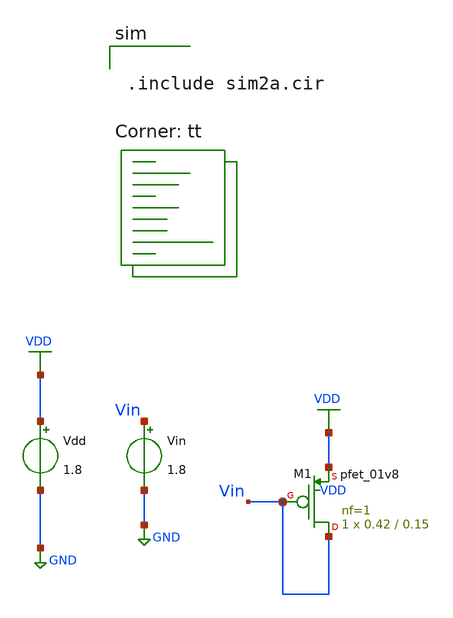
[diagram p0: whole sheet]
** sch_path: assignments/assignment1/assign2a.sch
**.subckt assign2a
Vdd VDD GND 1.8
XM1 Vin Vin VDD VDD sky130_fd_pr__pfet_01v8 L=0.15 W=0.42 nf=1 ad='int((nf+1)/2) * W/nf * 0.29' as='int((nf+2)/2) * W/nf * 0.29'
+ pd='2*int((nf+1)/2) * (W/nf + 0.29)' ps='2*int((nf+2)/2) * (W/nf + 0.29)' nrd='0.29 / W' nrs='0.29 / W'
+ sa=0 sb=0 sd=0 mult=1 m=1
Vin Vin GND 1.8
**** begin user architecture code


.include sim2a.cir


.lib $::SKYWATER_MODELS/sky130.lib.spice tt
**** end user architecture code
**.ends
.GLOBAL GND
.GLOBAL VDD
.end
